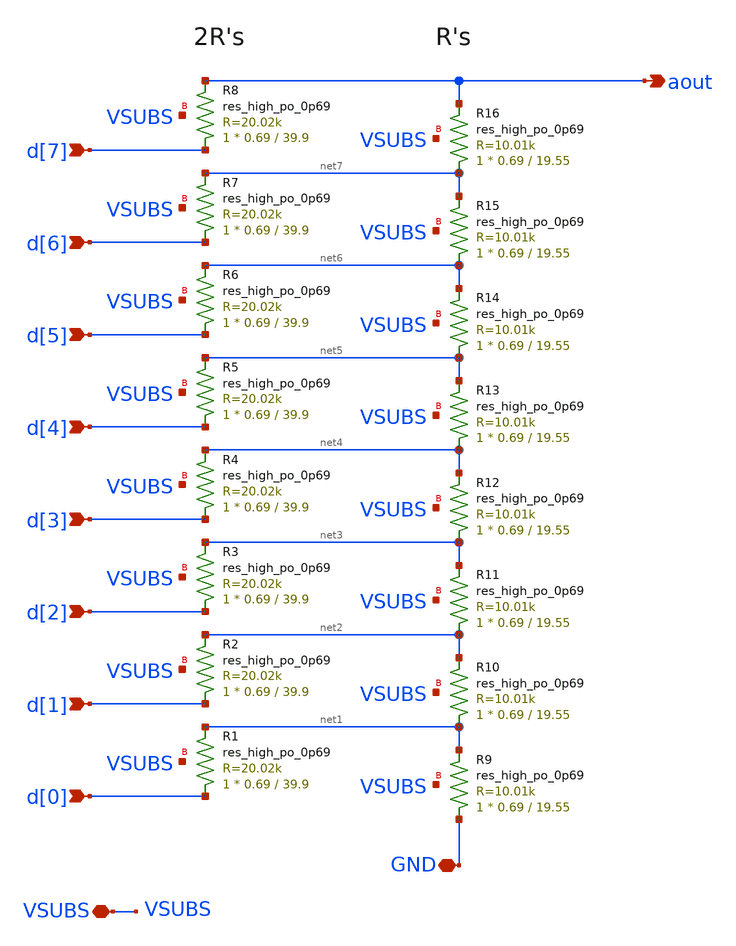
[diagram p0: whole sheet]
** sch_path: xschem/r2r.sch
**.subckt r2r d[0] d[1] d[2] d[3] d[4] d[5] d[6] d[7] GND VSUBS aout
*.ipin d[0]
*.ipin d[1]
*.ipin d[2]
*.ipin d[3]
*.ipin d[4]
*.ipin d[5]
*.ipin d[6]
*.ipin d[7]
*.iopin GND
*.iopin VSUBS
*.opin aout
XR1 d[0] net1 VSUBS sky130_fd_pr__res_high_po_0p69 L=39.9 mult=1 m=1
XR2 d[1] net2 VSUBS sky130_fd_pr__res_high_po_0p69 L=39.9 mult=1 m=1
XR3 d[2] net3 VSUBS sky130_fd_pr__res_high_po_0p69 L=39.9 mult=1 m=1
XR4 d[3] net4 VSUBS sky130_fd_pr__res_high_po_0p69 L=39.9 mult=1 m=1
XR5 d[4] net5 VSUBS sky130_fd_pr__res_high_po_0p69 L=39.9 mult=1 m=1
XR6 d[5] net6 VSUBS sky130_fd_pr__res_high_po_0p69 L=39.9 mult=1 m=1
XR7 d[6] net7 VSUBS sky130_fd_pr__res_high_po_0p69 L=39.9 mult=1 m=1
XR8 d[7] aout VSUBS sky130_fd_pr__res_high_po_0p69 L=39.9 mult=1 m=1
XR9 GND net1 VSUBS sky130_fd_pr__res_high_po_0p69 L=19.55 mult=1 m=1
XR10 net1 net2 VSUBS sky130_fd_pr__res_high_po_0p69 L=19.55 mult=1 m=1
XR11 net2 net3 VSUBS sky130_fd_pr__res_high_po_0p69 L=19.55 mult=1 m=1
XR12 net3 net4 VSUBS sky130_fd_pr__res_high_po_0p69 L=19.55 mult=1 m=1
XR13 net4 net5 VSUBS sky130_fd_pr__res_high_po_0p69 L=19.55 mult=1 m=1
XR14 net5 net6 VSUBS sky130_fd_pr__res_high_po_0p69 L=19.55 mult=1 m=1
XR15 net6 net7 VSUBS sky130_fd_pr__res_high_po_0p69 L=19.55 mult=1 m=1
XR16 net7 aout VSUBS sky130_fd_pr__res_high_po_0p69 L=19.55 mult=1 m=1
**.ends
.end
